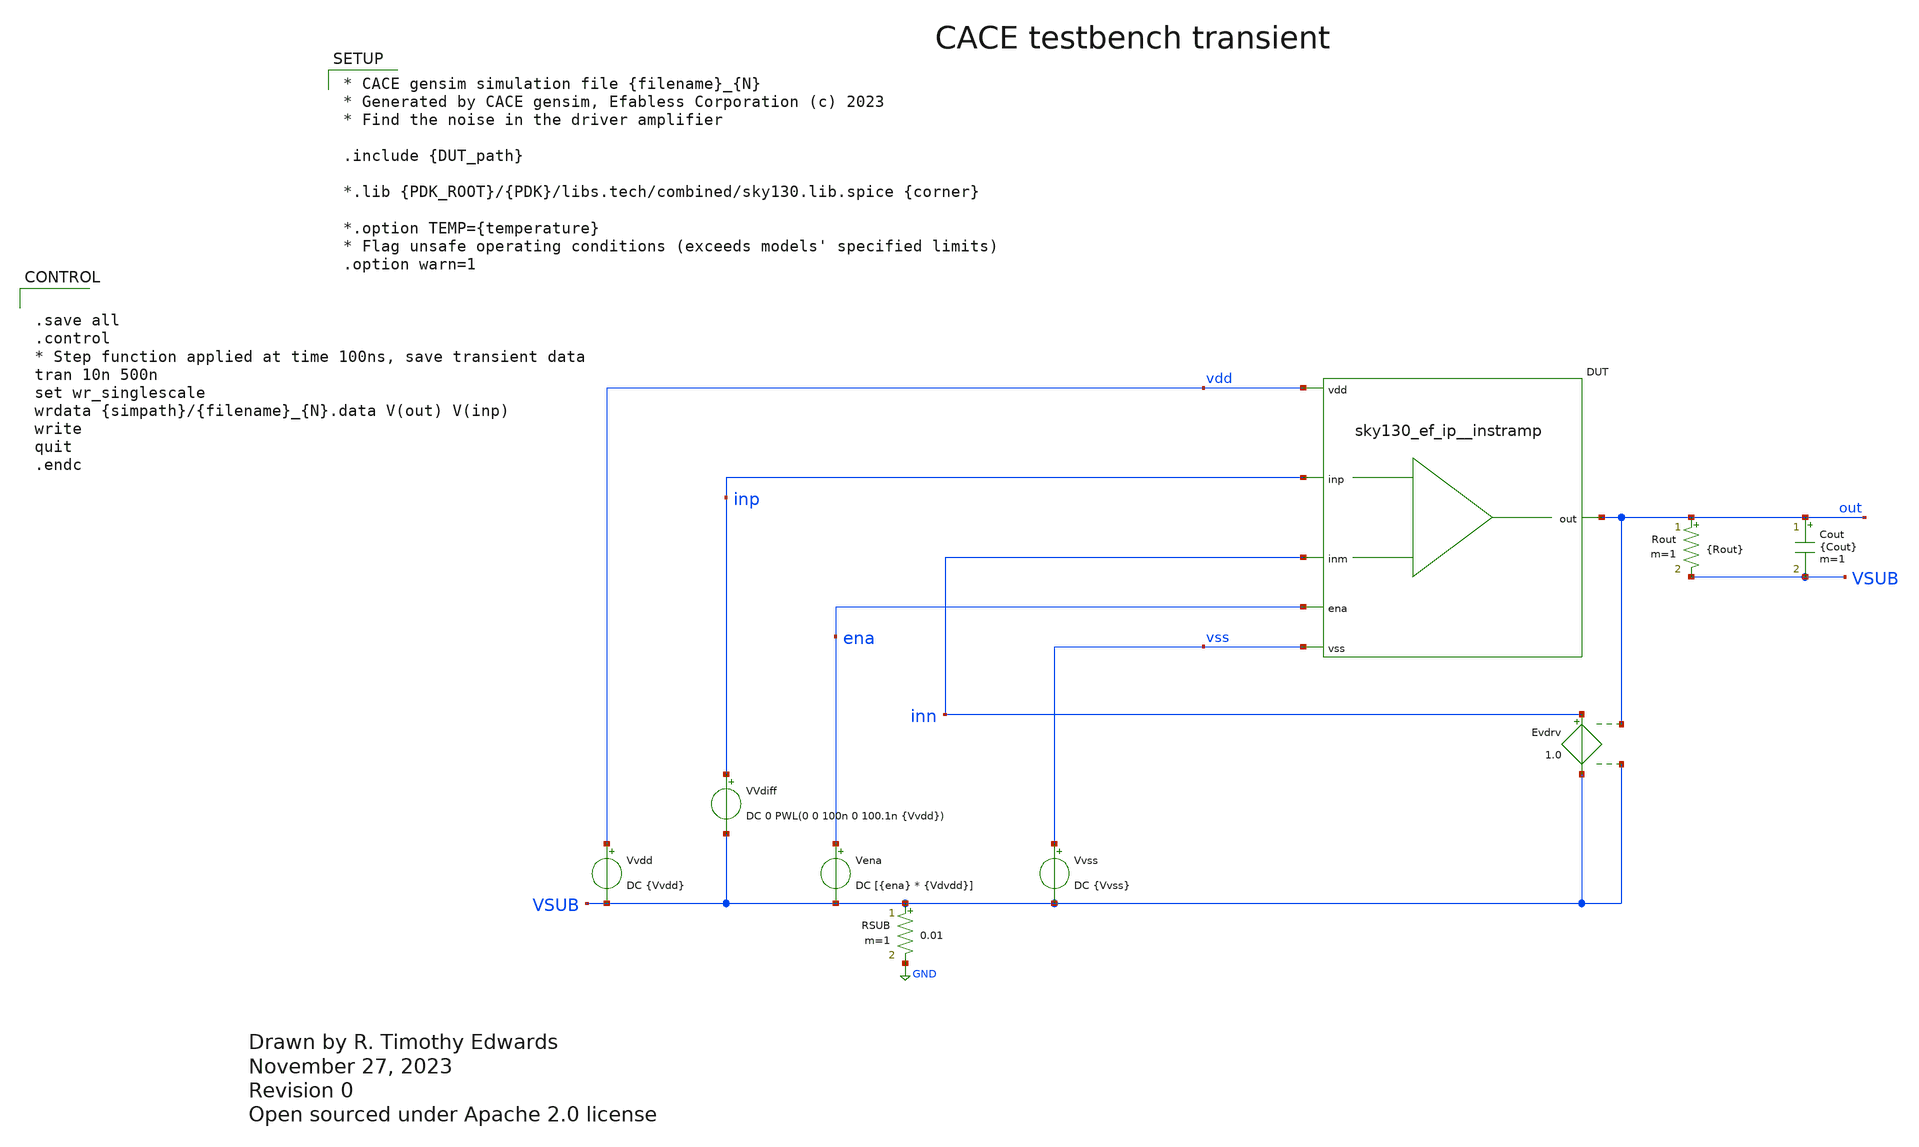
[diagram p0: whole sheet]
** sch_path: cace/transient.sch
* Open sourced under Apache 2.0 license
**.subckt transient
VVdiff inp VSUB DC 0 PWL(0 0 100n 0 100.1n {Vvdd})
Vena ena VSUB DC [{ena} * {Vdvdd}]
Vvss vss VSUB DC {Vvss}
Rout out VSUB {Rout} m=1
Cout out VSUB {Cout} m=1
Vvdd vdd VSUB DC {Vvdd}
RSUB VSUB GND 0.01 m=1
XDUT {PIN|vdd|vdd} {PIN|vss|vss} {PIN|inn|inm} {PIN|inp|inp} {PIN|out|out} {PIN|ena|ena} {DUT_name}
Evdrv inn VSUB out VSUB 1.0
**** begin user architecture code


.save all
.control
* Step function applied at time 100ns, save transient data
tran 10n 500n
set wr_singlescale
wrdata {simpath}/{filename}_{N}.data V(out) V(inp)
write
quit
.endc



* CACE gensim simulation file {filename}_{N}
* Generated by CACE gensim, Efabless Corporation (c) 2023
* Find the noise in the driver amplifier

.include {DUT_path}

*.lib {PDK_ROOT}/{PDK}/libs.tech/combined/sky130.lib.spice {corner}

*.option TEMP={temperature}
* Flag unsafe operating conditions (exceeds models' specified limits)
.option warn=1



**** end user architecture code
**.ends
.GLOBAL GND
.end
